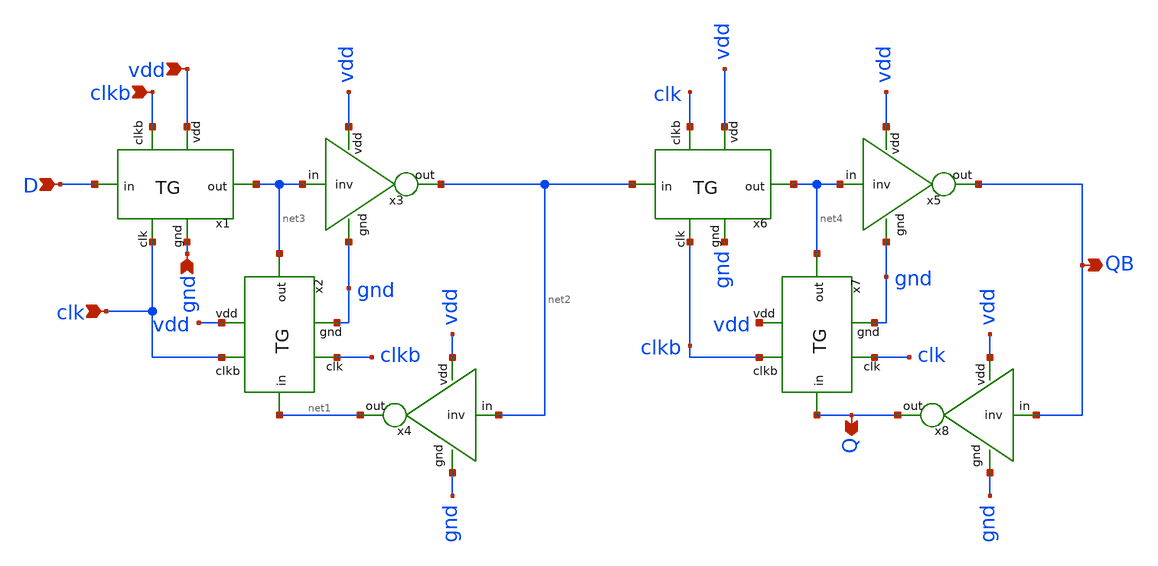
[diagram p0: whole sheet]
** sch_path: pll/dividers_lib/divider_design_trials/divider_2by3stages/DFF.sch
**.subckt DFF D clk clkb vdd gnd QB Q
*.ipin D
*.ipin clk
*.ipin clkb
*.ipin vdd
*.ipin gnd
*.opin QB
*.opin Q
x3 vdd net3 net2 gnd inv
x1 clk vdd D net3 gnd clkb TG
x2 clkb vdd net1 net3 gnd clk TG
x4 vdd net2 net1 gnd inv
x5 vdd net4 QB gnd inv
x6 clkb vdd net2 net4 gnd clk TG
x7 clk vdd Q net4 gnd clkb TG
x8 vdd QB Q gnd inv
**.ends
.end
